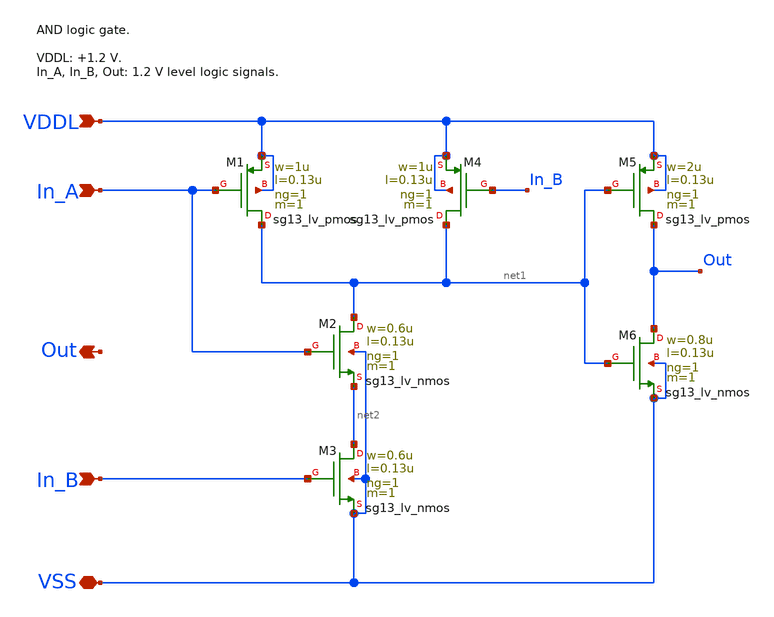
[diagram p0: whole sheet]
** sch_path: sar_adc/xschem/blocks/logic_elements/2-input_AND/2-input_AND.sch
**.subckt 2-input_AND Out VSS VDDL In_A In_B
*.opin Out
*.iopin VSS
*.ipin VDDL
*.ipin In_A
*.ipin In_B
XM1 net1 In_A VDDL VDDL sg13_lv_pmos w=1u l=0.13u ng=1 m=1 mm_ok=1
XM4 net1 In_B VDDL VDDL sg13_lv_pmos w=1u l=0.13u ng=1 m=1 mm_ok=1
XM2 net1 In_A net2 VSS sg13_lv_nmos w=0.6u l=0.13u ng=1 m=1 mm_ok=1
XM3 net2 In_B VSS VSS sg13_lv_nmos w=0.6u l=0.13u ng=1 m=1 mm_ok=1
XM5 Out net1 VDDL VDDL sg13_lv_pmos w=2u l=0.13u ng=1 m=1 mm_ok=1
XM6 Out net1 VSS VSS sg13_lv_nmos w=0.8u l=0.13u ng=1 m=1 mm_ok=1
**.ends
.end
